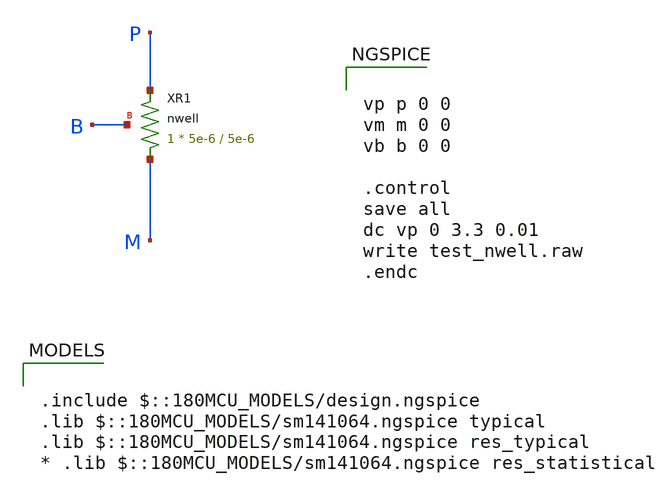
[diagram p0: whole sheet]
** sch_path: gf180mcuD/xschem_libs/gf180mcu_tests/test_nwell/schematic/test_nwell.sch
* Copyright 2022 GlobalFoundries PDK Authors
* Licensed under the Apache License, Version 2.0 (the "License");
* you may not use this file except in compliance with the License.
* You may obtain a copy of the License at
* https://www.apache.org/licenses/LICENSE-2.0
* Unless required by applicable law or agreed to in writing, software
* distributed under the License is distributed on an "AS IS" BASIS,
* WITHOUT WARRANTIES OR CONDITIONS OF ANY KIND, either express or implied.
* See the License for the specific language governing permissions and
* limitations under the License.
**.subckt test_nwell
XR1 M P B nwell r_width=5e-6 r_length=5e-6 m=1
**** begin user architecture code

.include $::180MCU_MODELS/design.ngspice
.lib $::180MCU_MODELS/sm141064.ngspice typical
.lib $::180MCU_MODELS/sm141064.ngspice res_typical
* .lib $::180MCU_MODELS/sm141064.ngspice res_statistical



vp p 0 0
vm m 0 0
vb b 0 0

.control
save all
dc vp 0 3.3 0.01
write test_nwell.raw
.endc


**** end user architecture code
**.ends
.end
